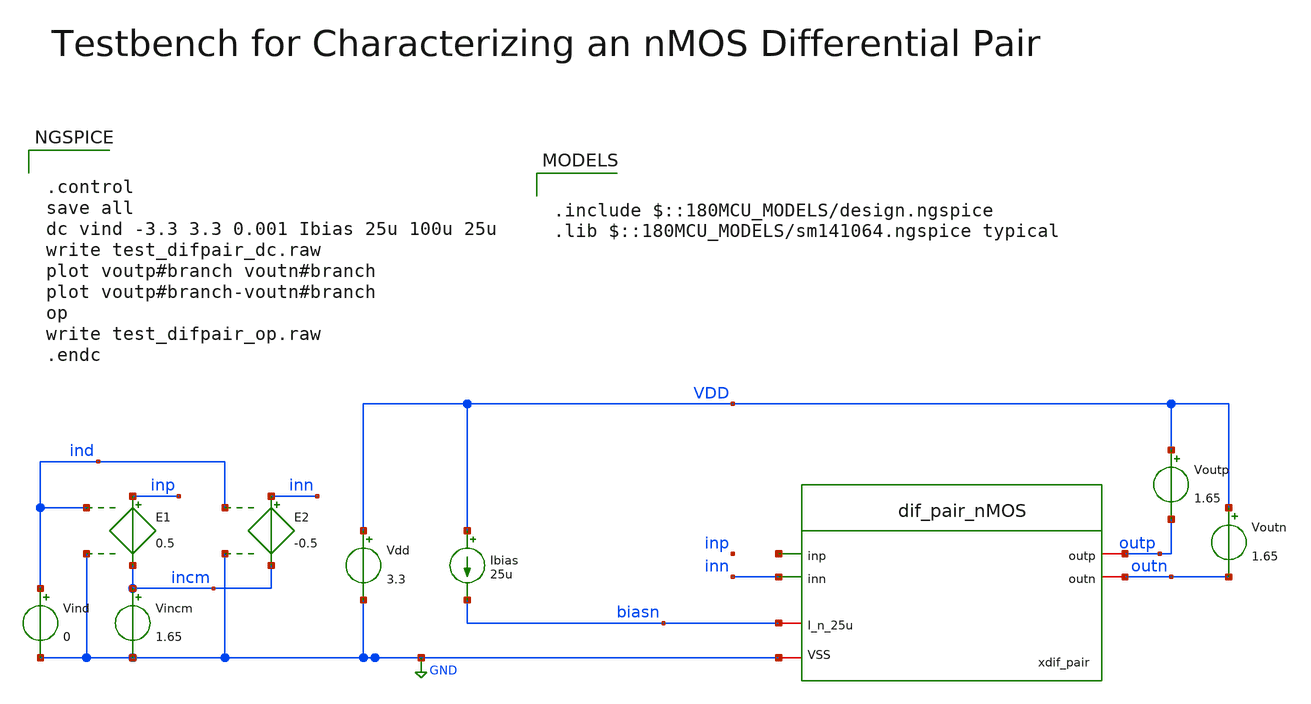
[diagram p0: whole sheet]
** sch_path: designs/libs/sandbox/dif_pair_nMOS_tb_w_graph.sch
**.subckt dif_pair_nMOS_tb_w_graph
xdif_pair outp outn net1 inn biasn GND dif_pair_nMOS
Ibias VDD biasn 25u
Voutp VDD outp 1.65
Voutn VDD outn 1.65
Vdd VDD GND 3.3
Vincm incm GND 1.65
Vind ind GND 0
E1 inp incm ind GND 0.5
E2 inn incm ind GND -0.5
**** begin user architecture code

.include $::180MCU_MODELS/design.ngspice
.lib $::180MCU_MODELS/sm141064.ngspice typical



.control
save all
dc vind -3.3 3.3 0.001 Ibias 25u 100u 25u
write test_difpair_dc.raw
plot voutp#branch voutn#branch
plot voutp#branch-voutn#branch
op
write test_difpair_op.raw
.endc


**** end user architecture code
**.ends

* expanding   symbol:  libs/sandbox/dif_pair_nMOS.sym # of pins=6
** sym_path: designs/libs/sandbox/dif_pair_nMOS.sym
** sch_path: designs/libs/sandbox/dif_pair_nMOS.sch
.subckt dif_pair_nMOS outp outn inp inn I_n_25u VSS
*.iopin outn
*.iopin outp
*.iopin I_n_25u
*.ipin inp
*.ipin inn
*.iopin VSS
XM1 outn inp cmsrc VSS nfet_03v3 L=0.28u W=3u nf=1 ad='int((nf+1)/2) * W/nf * 0.18u' as='int((nf+2)/2) * W/nf * 0.18u'
+ pd='2*int((nf+1)/2) * (W/nf + 0.18u)' ps='2*int((nf+2)/2) * (W/nf + 0.18u)' nrd='0.18u / W' nrs='0.18u / W'
+ sa=0 sb=0 sd=0 m=1
XM2 outp inn cmsrc VSS nfet_03v3 L=0.28u W=3u nf=1 ad='int((nf+1)/2) * W/nf * 0.18u' as='int((nf+2)/2) * W/nf * 0.18u'
+ pd='2*int((nf+1)/2) * (W/nf + 0.18u)' ps='2*int((nf+2)/2) * (W/nf + 0.18u)' nrd='0.18u / W' nrs='0.18u / W'
+ sa=0 sb=0 sd=0 m=1
XM3 cmsrc I_n_25u VSS VSS nfet_03v3 L=0.28u W=3u nf=1 ad='int((nf+1)/2) * W/nf * 0.18u' as='int((nf+2)/2) * W/nf * 0.18u'
+ pd='2*int((nf+1)/2) * (W/nf + 0.18u)' ps='2*int((nf+2)/2) * (W/nf + 0.18u)' nrd='0.18u / W' nrs='0.18u / W'
+ sa=0 sb=0 sd=0 m=2
XM4 I_n_25u I_n_25u VSS VSS nfet_03v3 L=0.28u W=3u nf=1 ad='int((nf+1)/2) * W/nf * 0.18u' as='int((nf+2)/2) * W/nf * 0.18u'
+ pd='2*int((nf+1)/2) * (W/nf + 0.18u)' ps='2*int((nf+2)/2) * (W/nf + 0.18u)' nrd='0.18u / W' nrs='0.18u / W'
+ sa=0 sb=0 sd=0 m=1
.ends

.GLOBAL GND
.end
